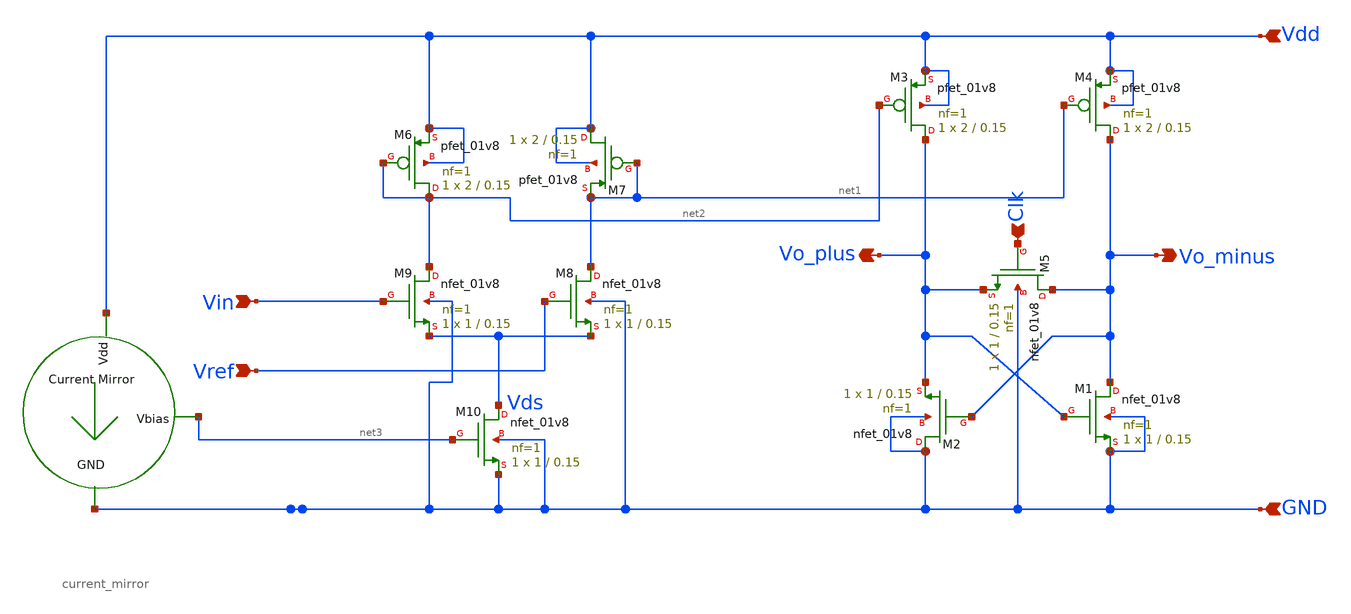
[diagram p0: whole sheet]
** sch_path: Comparator.sch
**.subckt Comparator Clk Vo_minus Vo_plus Vdd Vin Vref GND
*.ipin Clk
*.opin Vo_minus
*.opin Vo_plus
*.ipin Vdd
*.ipin Vin
*.ipin Vref
*.ipin GND
XM1 Vo_minus Vo_plus GND GND sky130_fd_pr__nfet_01v8 L=0.15 W=1 nf=1 ad='int((1 + 1)/2) * 1 / 1 * 0.29'
+ as='int((1 + 2)/2) * 1 / 1 * 0.29' pd='2*int((1 + 1)/2) * (1 / 1 + 0.29)' ps='2*int((1 + 2)/2) * (1 / 1 + 0.29)'
+ nrd='0.29 / 1 ' nrs='0.29 / 1 ' sa=0 sb=0 sd=0 mult=1 m=1
XM3 Vo_plus net2 Vdd Vdd sky130_fd_pr__pfet_01v8 L=0.15 W=2 nf=1 ad='int((1 + 1)/2) * 2 / 1 * 0.29' as='int((1 + 2)/2) * 2 / 1 * 0.29'
+ pd='2*int((1 + 1)/2) * (2 / 1 + 0.29)' ps='2*int((1 + 2)/2) * (2 / 1 + 0.29)' nrd='0.29 / 2 ' nrs='0.29 / 2 '
+ sa=0 sb=0 sd=0 mult=1 m=1
XM4 Vo_minus net1 Vdd Vdd sky130_fd_pr__pfet_01v8 L=0.15 W=2 nf=1 ad='int((1 + 1)/2) * 2 / 1 * 0.29'
+ as='int((1 + 2)/2) * 2 / 1 * 0.29' pd='2*int((1 + 1)/2) * (2 / 1 + 0.29)' ps='2*int((1 + 2)/2) * (2 / 1 + 0.29)'
+ nrd='0.29 / 2 ' nrs='0.29 / 2 ' sa=0 sb=0 sd=0 mult=1 m=1
XM2 GND Vo_minus Vo_plus GND sky130_fd_pr__nfet_01v8 L=0.15 W=1 nf=1 ad='int((1 + 1)/2) * 1 / 1 * 0.29'
+ as='int((1 + 2)/2) * 1 / 1 * 0.29' pd='2*int((1 + 1)/2) * (1 / 1 + 0.29)' ps='2*int((1 + 2)/2) * (1 / 1 + 0.29)'
+ nrd='0.29 / 1 ' nrs='0.29 / 1 ' sa=0 sb=0 sd=0 mult=1 m=1
XM5 Vo_minus Clk Vo_plus GND sky130_fd_pr__nfet_01v8 L=0.15 W=1 nf=1 ad='int((1 + 1)/2) * 1 / 1 * 0.29'
+ as='int((1 + 2)/2) * 1 / 1 * 0.29' pd='2*int((1 + 1)/2) * (1 / 1 + 0.29)' ps='2*int((1 + 2)/2) * (1 / 1 + 0.29)'
+ nrd='0.29 / 1 ' nrs='0.29 / 1 ' sa=0 sb=0 sd=0 mult=1 m=1
XM6 net2 net2 Vdd Vdd sky130_fd_pr__pfet_01v8 L=0.15 W=2 nf=1 ad='int((1 + 1)/2) * 2 / 1 * 0.29' as='int((1 + 2)/2) * 2 / 1 * 0.29'
+ pd='2*int((1 + 1)/2) * (2 / 1 + 0.29)' ps='2*int((1 + 2)/2) * (2 / 1 + 0.29)' nrd='0.29 / 2 ' nrs='0.29 / 2 '
+ sa=0 sb=0 sd=0 mult=1 m=1
XM7 Vdd net1 net1 Vdd sky130_fd_pr__pfet_01v8 L=0.15 W=2 nf=1 ad='int((1 + 1)/2) * 2 / 1 * 0.29' as='int((1 + 2)/2) * 2 / 1 * 0.29'
+ pd='2*int((1 + 1)/2) * (2 / 1 + 0.29)' ps='2*int((1 + 2)/2) * (2 / 1 + 0.29)' nrd='0.29 / 2 ' nrs='0.29 / 2 '
+ sa=0 sb=0 sd=0 mult=1 m=1
XM8 net1 Vref Vds GND sky130_fd_pr__nfet_01v8 L=0.15 W=1 nf=1 ad='int((1 + 1)/2) * 1 / 1 * 0.29' as='int((1 + 2)/2) * 1 / 1 * 0.29'
+ pd='2*int((1 + 1)/2) * (1 / 1 + 0.29)' ps='2*int((1 + 2)/2) * (1 / 1 + 0.29)' nrd='0.29 / 1 ' nrs='0.29 / 1 '
+ sa=0 sb=0 sd=0 mult=1 m=1
XM9 net2 Vin Vds GND sky130_fd_pr__nfet_01v8 L=0.15 W=1 nf=1 ad='int((1 + 1)/2) * 1 / 1 * 0.29' as='int((1 + 2)/2) * 1 / 1 * 0.29'
+ pd='2*int((1 + 1)/2) * (1 / 1 + 0.29)' ps='2*int((1 + 2)/2) * (1 / 1 + 0.29)' nrd='0.29 / 1 ' nrs='0.29 / 1 '
+ sa=0 sb=0 sd=0 mult=1 m=1
XM10 Vds net3 GND GND sky130_fd_pr__nfet_01v8 L=0.15 W=1 nf=1 ad='int((1 + 1)/2) * 1 / 1 * 0.29' as='int((1 + 2)/2) * 1 / 1 * 0.29'
+ pd='2*int((1 + 1)/2) * (1 / 1 + 0.29)' ps='2*int((1 + 2)/2) * (1 / 1 + 0.29)' nrd='0.29 / 1 ' nrs='0.29 / 1 '
+ sa=0 sb=0 sd=0 mult=1 m=1
x1 Vdd net3 GND current_mirror
**.ends

* expanding   symbol:  current_mirror.sym # of pins=3
** sym_path: current_mirror.sym
** sch_path: current_mirror.sch
.subckt current_mirror Vdd Vbias GND
*.ipin GND
*.opin Vbias
*.ipin Vdd
R2 Vdd Vbias 180k m=1
XM3 Vbias Vbias GND GND sky130_fd_pr__nfet_01v8 L=0.15 W=1 nf=1 ad='int((1 + 1)/2) * 1 / 1 * 0.29' as='int((1 + 2)/2) * 1 / 1 * 0.29'
+ pd='2*int((1 + 1)/2) * (1 / 1 + 0.29)' ps='2*int((1 + 2)/2) * (1 / 1 + 0.29)' nrd='0.29 / 1 ' nrs='0.29 / 1 '
+ sa=0 sb=0 sd=0 mult=1 m=1
.ends

.end
